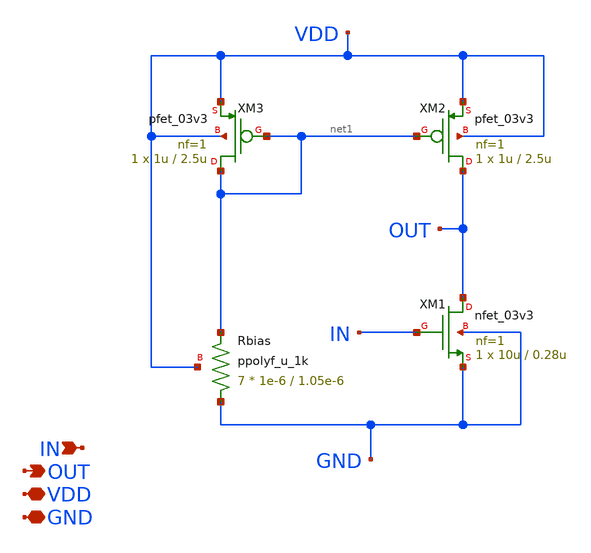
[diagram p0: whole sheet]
** sch_path: core_amp.sch
**.subckt core_amp IN OUT VDD GND
*.ipin IN
*.opin OUT
*.iopin VDD
*.iopin GND
XM1 OUT IN GND GND nfet_03v3 L=0.28u W=10u nf=1 ad='int((nf+1)/2) * W/nf * 0.18u' as='int((nf+2)/2) * W/nf * 0.18u'
+ pd='2*int((nf+1)/2) * (W/nf + 0.18u)' ps='2*int((nf+2)/2) * (W/nf + 0.18u)' nrd='0.18u / W' nrs='0.18u / W'
+ sa=0 sb=0 sd=0 m=1
XM2 OUT net1 VDD VDD pfet_03v3 L=2.5u W=1u nf=1 ad='int((nf+1)/2) * W/nf * 0.18u' as='int((nf+2)/2) * W/nf * 0.18u'
+ pd='2*int((nf+1)/2) * (W/nf + 0.18u)' ps='2*int((nf+2)/2) * (W/nf + 0.18u)' nrd='0.18u / W' nrs='0.18u / W'
+ sa=0 sb=0 sd=0 m=1
XM3 net1 net1 VDD VDD pfet_03v3 L=2.5u W=1u nf=1 ad='int((nf+1)/2) * W/nf * 0.18u' as='int((nf+2)/2) * W/nf * 0.18u'
+ pd='2*int((nf+1)/2) * (W/nf + 0.18u)' ps='2*int((nf+2)/2) * (W/nf + 0.18u)' nrd='0.18u / W' nrs='0.18u / W'
+ sa=0 sb=0 sd=0 m=1
XRbias GND net1 VDD ppolyf_u_1k r_width=1e-6 r_length=1.05e-6 m=7
**.ends
.end
